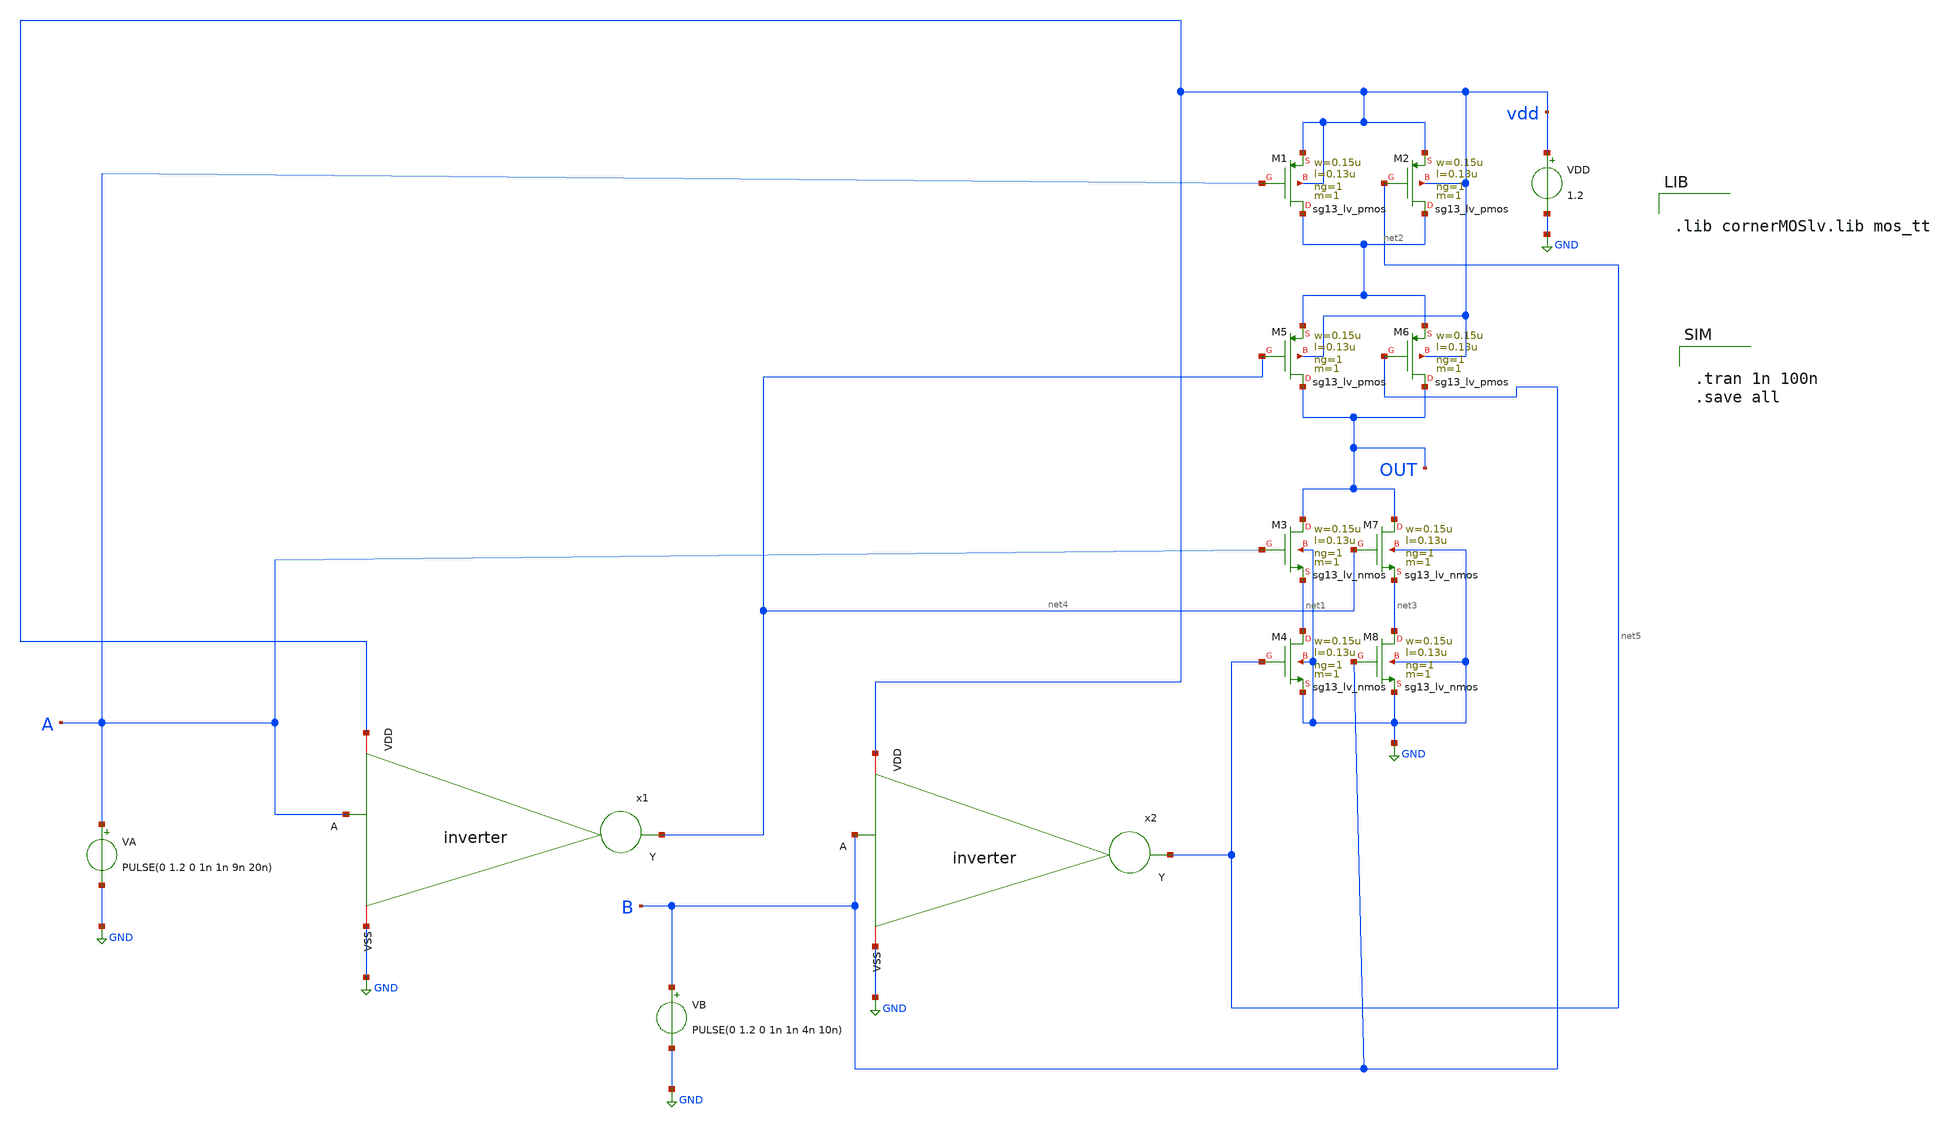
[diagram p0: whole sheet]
** sch_path: xnor.sch
**.subckt xnor
XM1 net2 A vdd vdd sg13_lv_pmos w=0.15u l=0.13u ng=1 m=1 mm_ok=1
XM2 net2 net5 vdd vdd sg13_lv_pmos w=0.15u l=0.13u ng=1 m=1 mm_ok=1
XM3 OUT A net1 GND sg13_lv_nmos w=0.15u l=0.13u ng=1 m=1 mm_ok=1
XM4 net1 net5 GND GND sg13_lv_nmos w=0.15u l=0.13u ng=1 m=1 mm_ok=1
VDD vdd GND 1.2
VA A GND PULSE(0 1.2 0 1n 1n 9n 20n)
VB B GND PULSE(0 1.2 0 1n 1n 4n 10n)
XM5 OUT net4 net2 vdd sg13_lv_pmos w=0.15u l=0.13u ng=1 m=1 mm_ok=1
XM6 OUT B net2 vdd sg13_lv_pmos w=0.15u l=0.13u ng=1 m=1 mm_ok=1
XM7 OUT net4 net3 GND sg13_lv_nmos w=0.15u l=0.13u ng=1 m=1 mm_ok=1
XM8 net3 B GND GND sg13_lv_nmos w=0.15u l=0.13u ng=1 m=1 mm_ok=1
x1 vdd A net4 GND inverter
x2 vdd B net5 GND inverter
**** begin user architecture code


.lib cornerMOSlv.lib mos_tt



.tran 1n 100n
.save all


**** end user architecture code
**.ends

* expanding   symbol:  xchem/xchem/inverter.sym # of pins=4
** sym_path: inverter.sym
** sch_path: inverter.sch
.subckt inverter VDD A Y VSS
*.ipin A
*.iopin VDD
*.iopin VSS
*.opin Y
XM1 Y A VDD VDD sg13_lv_pmos w=0.15u l=0.13u ng=1 m=1 mm_ok=1
XM2 Y A VSS VSS sg13_lv_nmos w=0.15u l=0.13u ng=1 m=1 mm_ok=1
.ends

.GLOBAL GND
.end
